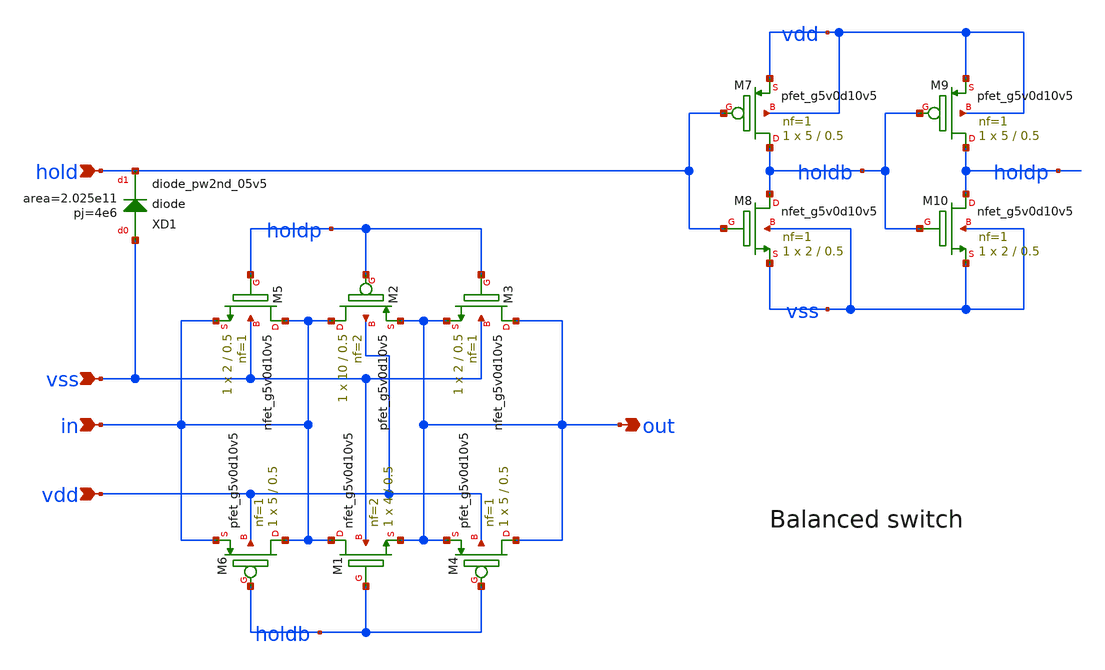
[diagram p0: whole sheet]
** sch_path: xschem/balanced_switch.sch
**.subckt balanced_switch in out vss vdd hold
*.ipin in
*.opin out
*.ipin vss
*.ipin vdd
*.ipin hold
XM1 in holdb out vss sky130_fd_pr__nfet_g5v0d10v5 L=0.5 W=4 nf=2 ad='int((nf+1)/2) * W/nf * 0.29' as='int((nf+2)/2) * W/nf * 0.29'
+ pd='2*int((nf+1)/2) * (W/nf + 0.29)' ps='2*int((nf+2)/2) * (W/nf + 0.29)' nrd='0.29 / W' nrs='0.29 / W'
+ sa=0 sb=0 sd=0 mult=1 m=1
XM2 in holdp out vdd sky130_fd_pr__pfet_g5v0d10v5 L=0.5 W=10 nf=2 ad='int((nf+1)/2) * W/nf * 0.29' as='int((nf+2)/2) * W/nf * 0.29'
+ pd='2*int((nf+1)/2) * (W/nf + 0.29)' ps='2*int((nf+2)/2) * (W/nf + 0.29)' nrd='0.29 / W' nrs='0.29 / W'
+ sa=0 sb=0 sd=0 mult=1 m=1
XM3 out holdp out vss sky130_fd_pr__nfet_g5v0d10v5 L=0.5 W=2 nf=1 ad='int((nf+1)/2) * W/nf * 0.29' as='int((nf+2)/2) * W/nf * 0.29'
+ pd='2*int((nf+1)/2) * (W/nf + 0.29)' ps='2*int((nf+2)/2) * (W/nf + 0.29)' nrd='0.29 / W' nrs='0.29 / W'
+ sa=0 sb=0 sd=0 mult=1 m=1
XM4 out holdb out vdd sky130_fd_pr__pfet_g5v0d10v5 L=0.5 W=5 nf=1 ad='int((nf+1)/2) * W/nf * 0.29' as='int((nf+2)/2) * W/nf * 0.29'
+ pd='2*int((nf+1)/2) * (W/nf + 0.29)' ps='2*int((nf+2)/2) * (W/nf + 0.29)' nrd='0.29 / W' nrs='0.29 / W'
+ sa=0 sb=0 sd=0 mult=1 m=1
XM5 in holdp in vss sky130_fd_pr__nfet_g5v0d10v5 L=0.5 W=2 nf=1 ad='int((nf+1)/2) * W/nf * 0.29' as='int((nf+2)/2) * W/nf * 0.29'
+ pd='2*int((nf+1)/2) * (W/nf + 0.29)' ps='2*int((nf+2)/2) * (W/nf + 0.29)' nrd='0.29 / W' nrs='0.29 / W'
+ sa=0 sb=0 sd=0 mult=1 m=1
XM6 in holdb in vdd sky130_fd_pr__pfet_g5v0d10v5 L=0.5 W=5 nf=1 ad='int((nf+1)/2) * W/nf * 0.29' as='int((nf+2)/2) * W/nf * 0.29'
+ pd='2*int((nf+1)/2) * (W/nf + 0.29)' ps='2*int((nf+2)/2) * (W/nf + 0.29)' nrd='0.29 / W' nrs='0.29 / W'
+ sa=0 sb=0 sd=0 mult=1 m=1
XM7 holdb hold vdd vdd sky130_fd_pr__pfet_g5v0d10v5 L=0.5 W=5 nf=1 ad='int((nf+1)/2) * W/nf * 0.29' as='int((nf+2)/2) * W/nf * 0.29'
+ pd='2*int((nf+1)/2) * (W/nf + 0.29)' ps='2*int((nf+2)/2) * (W/nf + 0.29)' nrd='0.29 / W' nrs='0.29 / W'
+ sa=0 sb=0 sd=0 mult=1 m=1
XM8 holdb hold vss vss sky130_fd_pr__nfet_g5v0d10v5 L=0.5 W=2 nf=1 ad='int((nf+1)/2) * W/nf * 0.29' as='int((nf+2)/2) * W/nf * 0.29'
+ pd='2*int((nf+1)/2) * (W/nf + 0.29)' ps='2*int((nf+2)/2) * (W/nf + 0.29)' nrd='0.29 / W' nrs='0.29 / W'
+ sa=0 sb=0 sd=0 mult=1 m=1
XM9 holdp holdb vdd vdd sky130_fd_pr__pfet_g5v0d10v5 L=0.5 W=5 nf=1 ad='int((nf+1)/2) * W/nf * 0.29'
+ as='int((nf+2)/2) * W/nf * 0.29' pd='2*int((nf+1)/2) * (W/nf + 0.29)' ps='2*int((nf+2)/2) * (W/nf + 0.29)'
+ nrd='0.29 / W' nrs='0.29 / W' sa=0 sb=0 sd=0 mult=1 m=1
XM10 holdp holdb vss vss sky130_fd_pr__nfet_g5v0d10v5 L=0.5 W=2 nf=1 ad='int((nf+1)/2) * W/nf * 0.29'
+ as='int((nf+2)/2) * W/nf * 0.29' pd='2*int((nf+1)/2) * (W/nf + 0.29)' ps='2*int((nf+2)/2) * (W/nf + 0.29)'
+ nrd='0.29 / W' nrs='0.29 / W' sa=0 sb=0 sd=0 mult=1 m=1
XXD1 vss hold sky130_fd_pr__diode_pw2nd_05v5 area=2.025e11 pj=4e6
**.ends
.end
